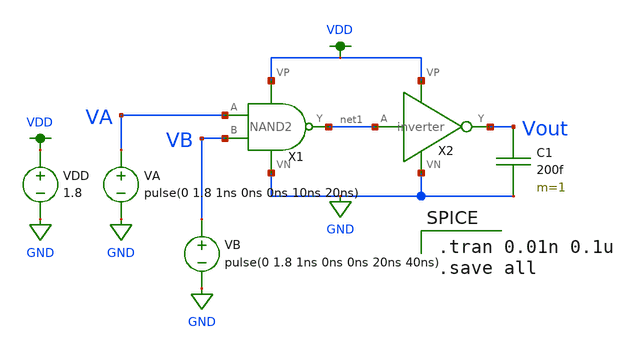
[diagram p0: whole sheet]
** sch_path: mini1/schem/AND.sch
**.subckt AND
C1 Vout GND 200f m=1
VA VA GND pulse(0 1.8 1ns 0ns 0ns 10ns 20ns)
VB VB GND pulse(0 1.8 1ns 0ns 0ns 20ns 40ns)
VDD VDD GND 1.8
X1 net1 GND VDD VA VB NAND2
X2 net1 Vout VDD GND inverter
**** begin user architecture code

.option wnflag=1
.lib ~/skywater/skywater-pdk/libraries/sky130_fd_pr_ngspice/latest/models/sky130.lib.spice tt


.tran 0.01n 0.1u
.save all

**** end user architecture code
**.ends
.GLOBAL VDD
.GLOBAL GND
.end
